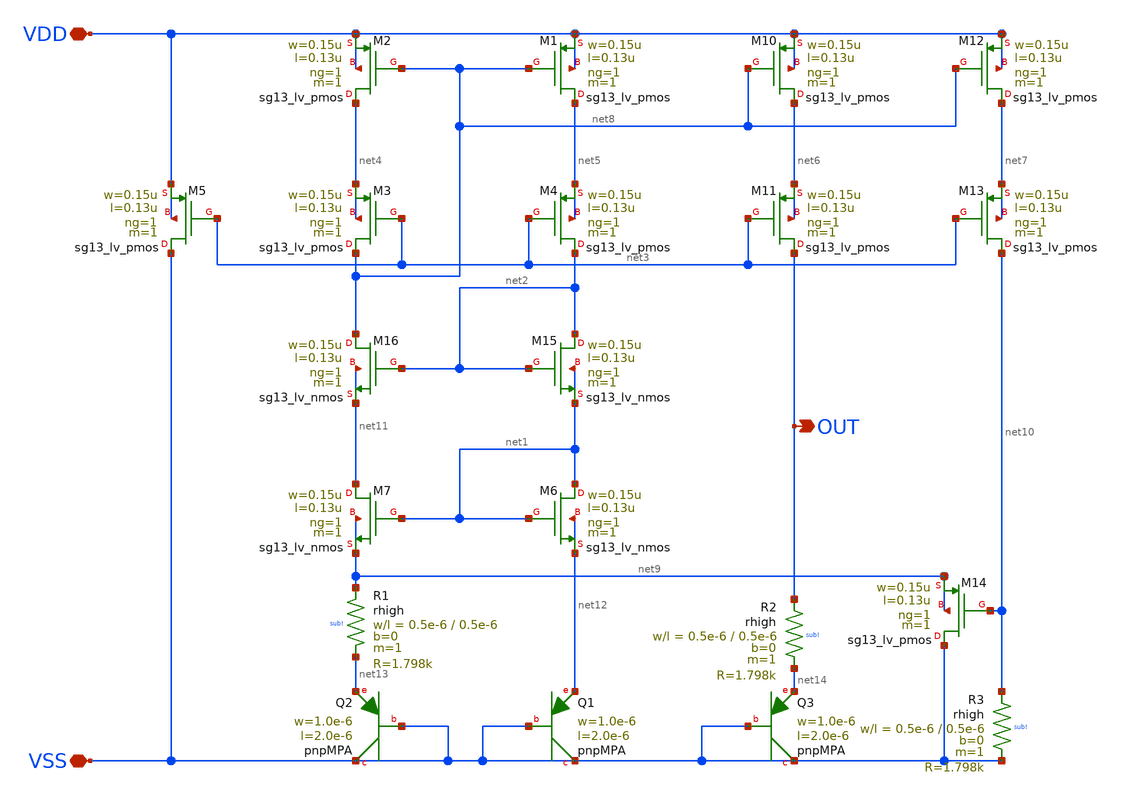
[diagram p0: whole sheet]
** sch_path: libs/core_analog/core_bandgap/schematics/core-bandgap.sch
**.subckt core-bandgap VDD VSS OUT
*.iopin VDD
*.iopin VSS
*.opin OUT
XM1 net5 net8 VDD VDD sg13_lv_pmos w=0.15u l=0.13u ng=1 m=1 mm_ok=1
XM2 net4 net8 VDD VDD sg13_lv_pmos w=0.15u l=0.13u ng=1 m=1 mm_ok=1
XM3 net8 net3 net4 net4 sg13_lv_pmos w=0.15u l=0.13u ng=1 m=1 mm_ok=1
XM4 net2 net3 net5 net5 sg13_lv_pmos w=0.15u l=0.13u ng=1 m=1 mm_ok=1
XM5 VSS net3 VDD VDD sg13_lv_pmos w=0.15u l=0.13u ng=1 m=1 mm_ok=1
XM10 net6 net8 VDD VDD sg13_lv_pmos w=0.15u l=0.13u ng=1 m=1 mm_ok=1
XM11 OUT net3 net6 net6 sg13_lv_pmos w=0.15u l=0.13u ng=1 m=1 mm_ok=1
XM12 net7 net8 VDD VDD sg13_lv_pmos w=0.15u l=0.13u ng=1 m=1 mm_ok=1
XM13 net10 net3 net7 net7 sg13_lv_pmos w=0.15u l=0.13u ng=1 m=1 mm_ok=1
XR1 net9 net13 sub! rhigh w=0.5e-6 l=0.5e-6 m=1 b=0 mm_ok=1
XQ1 VSS VSS net12 pnpMPA a=2p p=6u m=1
XQ2 VSS VSS net13 pnpMPA a=2p p=6u m=1
XQ3 VSS VSS net14 pnpMPA a=2p p=6u m=1
XR2 OUT net14 sub! rhigh w=0.5e-6 l=0.5e-6 m=1 b=0 mm_ok=1
XM14 VSS net10 net9 net9 sg13_lv_pmos w=0.15u l=0.13u ng=1 m=1 mm_ok=1
XR3 net10 VSS sub! rhigh w=0.5e-6 l=0.5e-6 m=1 b=0 mm_ok=1
XM15 net2 net2 net1 net1 sg13_lv_nmos w=0.15u l=0.13u ng=1 m=1 mm_ok=1
XM16 net8 net2 net11 net11 sg13_lv_nmos w=0.15u l=0.13u ng=1 m=1 mm_ok=1
XM6 net1 net1 net12 net12 sg13_lv_nmos w=0.15u l=0.13u ng=1 m=1 mm_ok=1
XM7 net11 net1 net9 net9 sg13_lv_nmos w=0.15u l=0.13u ng=1 m=1 mm_ok=1
**.ends
.end
